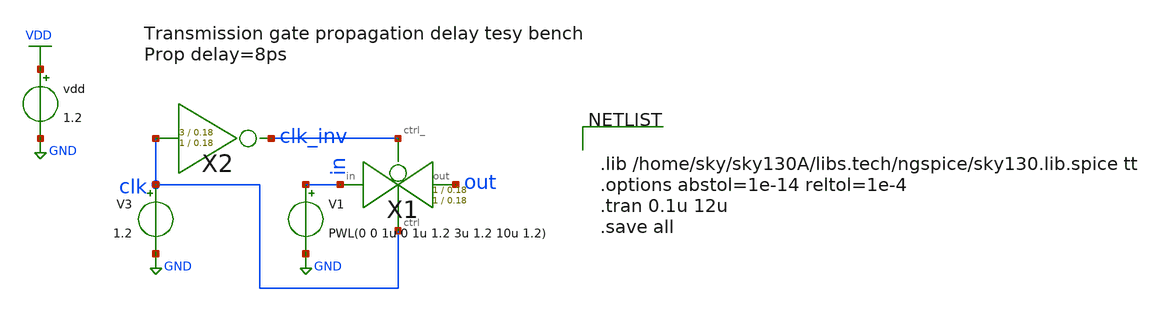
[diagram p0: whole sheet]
** sch_path: xschem/D_flip_flop/Transmission_gate_prop_delay_tb.sch
**.subckt Transmission_gate_prop_delay_tb
X1 in out clk_inv clk transmission_gate Wpmos=1 Lpmos=0.18 Wnmos=1 Lnmos=0.18
V1 in GND PWL(0 0 1u 0 1u 1.2 3u 1.2 10u 1.2)
V3 clk GND 1.2
X2 clk clk_inv inv Wpmos=3 Lpmos=0.18 Wnmos=1 Lnmos=0.18
vdd VDD GND 1.2
**** begin user architecture code


.lib /home/sky/sky130A/libs.tech/ngspice/sky130.lib.spice tt
.options abstol=1e-14 reltol=1e-4
.tran 0.1u 12u
.save all


**** end user architecture code
**.ends

* expanding   symbol:  transmission_gate/transmission_gate.sym # of pins=4
** sym_path: xschem/transmission_gate/transmission_gate.sym
** sch_path: xschem/transmission_gate/transmission_gate.sch
.subckt transmission_gate in out ctrl_ ctrl  Wpmos=1 Lpmos=0.18 Wnmos=1 Lnmos=0.18
*.iopin in
*.iopin out
*.ipin ctrl_
*.ipin ctrl
XM1 in ctrl out GND sky130_fd_pr__nfet_01v8 L=Lnmos W=Wnmos nf=1 ad='int((nf+1)/2) * W/nf * 0.29' as='int((nf+2)/2) * W/nf * 0.29'
+ pd='2*int((nf+1)/2) * (W/nf + 0.29)' ps='2*int((nf+2)/2) * (W/nf + 0.29)' nrd='0.29 / W' nrs='0.29 / W'
+ sa=0 sb=0 sd=0 mult=1 m=1
XM2 out ctrl_ in VDD sky130_fd_pr__pfet_01v8 L=Lpmos W=Wpmos nf=1 ad='int((nf+1)/2) * W/nf * 0.29' as='int((nf+2)/2) * W/nf * 0.29'
+ pd='2*int((nf+1)/2) * (W/nf + 0.29)' ps='2*int((nf+2)/2) * (W/nf + 0.29)' nrd='0.29 / W' nrs='0.29 / W'
+ sa=0 sb=0 sd=0 mult=1 m=1
.ends


* expanding   symbol:  inv/inv.sym # of pins=2
** sym_path: xschem/inv/inv.sym
** sch_path: xschem/inv/inv.sch
.subckt inv in out  Wpmos=3 Lpmos=0.18 Wnmos=1 Lnmos=0.18
*.ipin in
*.iopin out
XM1 out in GND GND sky130_fd_pr__nfet_01v8 L=Lnmos W=Wnmos nf=1 ad='int((nf+1)/2) * W/nf * 0.29' as='int((nf+2)/2) * W/nf * 0.29'
+ pd='2*int((nf+1)/2) * (W/nf + 0.29)' ps='2*int((nf+2)/2) * (W/nf + 0.29)' nrd='0.29 / W' nrs='0.29 / W'
+ sa=0 sb=0 sd=0 mult=1 m=1
XM2 out in VDD VDD sky130_fd_pr__pfet_01v8 L=Lpmos W=Wpmos nf=1 ad='int((nf+1)/2) * W/nf * 0.29' as='int((nf+2)/2) * W/nf * 0.29'
+ pd='2*int((nf+1)/2) * (W/nf + 0.29)' ps='2*int((nf+2)/2) * (W/nf + 0.29)' nrd='0.29 / W' nrs='0.29 / W'
+ sa=0 sb=0 sd=0 mult=1 m=1
.ends

.GLOBAL GND
.GLOBAL VDD
.end
